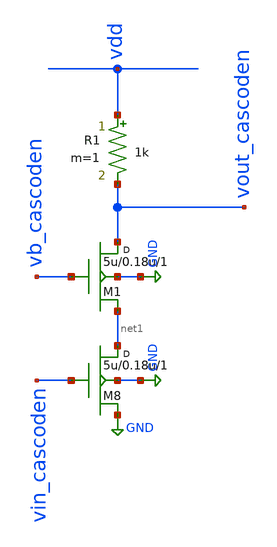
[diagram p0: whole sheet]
** sch_path: synthetic/blocks/cascode_nmos.sch
**.subckt cascode_nmos
M8 net1 vin_cascoden GND GND nmos w=5u l=0.18u m=1
M1 vout_cascoden vb_cascoden net1 GND nmos w=5u l=0.18u m=1
R1 vdd vout_cascoden 1k m=1
**.ends
.GLOBAL GND
.end
